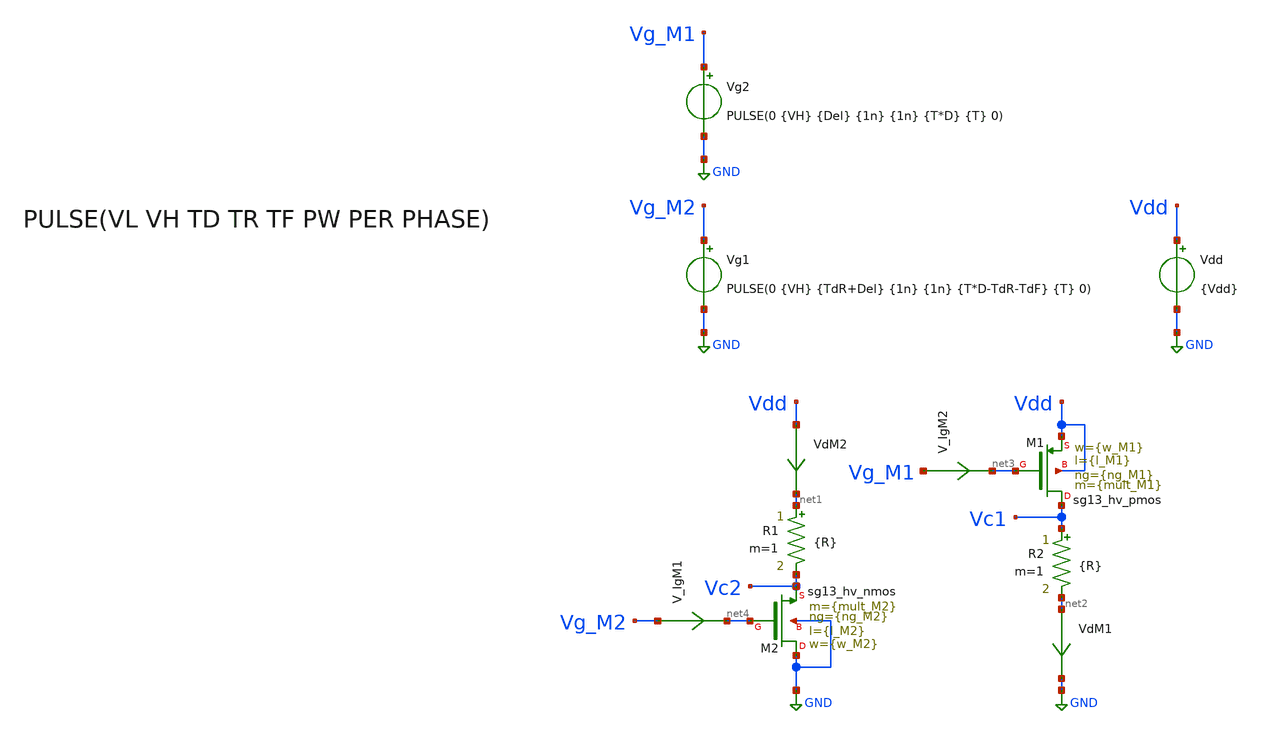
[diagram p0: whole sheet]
** sch_path: ChipUSM_AnalogTrack24/TestBenchs/TB_hvMOS_switch_test.sch
**.subckt TB_hvMOS_switch_test
XM2 GND net4 Vc2 GND sg13_hv_nmos w={w_M2} l={l_M2} ng={ng_M2} m={mult_M2} mm_ok=1
XM1 Vc1 net3 Vdd Vdd sg13_hv_pmos w={w_M1} l={l_M1} ng={ng_M1} m={mult_M1} mm_ok=1
Vdd Vdd GND {Vdd}
VdM2 Vdd net1 0
.save i(vdm2)
VdM1 net2 GND 0
.save i(vdm1)
Vg1 Vg_M2 GND PULSE(0 {VH} {TdR+Del} {1n} {1n} {T*D-TdR-TdF} {T} 0)
Vg2 Vg_M1 GND PULSE(0 {VH} {Del} {1n} {1n} {T*D} {T} 0)
R1 net1 Vc2 {R} m=1
R2 Vc1 net2 {R} m=1
V_IgM1 Vg_M2 net4 0
.save i(v_igm1)
V_IgM2 Vg_M1 net3 0
.save i(v_igm2)
**** begin user architecture code

.lib cornerMOShv.lib mos_tt



.param Vdd = 3.3
.param R = 0
.param VH = 0
* Ciclo de trabajo
.param D = 0.5

*Seteo de periodo
.param T = 0

.param TR = 1n
.param TF = 1n

*Tiempo muerto Rise
.param TdR = 0
*Tiempo muerto Fall
.param TdF = 0
*Delay de señal
.param Del = 0

.option temp = 27






.save all
.control
reset
set color0 = white
tran 1n 1u
let VsdM1 = v(Vdd) - v(Vc1)
let VdsM2 = v(Vc2)
plot i(VdM1) i(VdM2)
plot v(Vc1) v(Vc2)
plot v(Vg_M1) v(Vg_M2)
plot VsdM1 VdsM2
plot i(V_IgM1) i(V_IgM2)
meas TRAN td_off_M1 TRIG v(Vg_M1) VAL=0.33 RISE=1 TARG VsdM1 VAL=0.33 RISE=1
meas TRAN td_on_M1 TRIG v(Vg_M1) VAL=2.97 FALL=1 TARG VsdM1 VAL=2.97 FALL=1
meas TRAN td_on_M2 TRIG v(Vg_M2) VAL=0.33 RISE=1 TARG VdsM2 VAL=2.97 FALL=1
meas TRAN td_off_M2 TRIG v(Vg_M2) VAL=2.97 FALL=1 TARG VdsM2 VAL=0.33 RISE=1
let TdR = td_off_M1 - td_on_M2
let TdF = td_on_M1 - td_off_M2
print TdR TdF
.endc

.end




.param temp=27
.param mult_M1 = 1
.param w_M1 =0.3u
.param l_M1 = 0.4u
.param ng_M1 = 1

.param mult_M2 = 1
.param w_M2 =0.3u
.param l_M2 =0.45u
.param ng_M2 =1





**** end user architecture code
**.ends
.GLOBAL GND
.end
